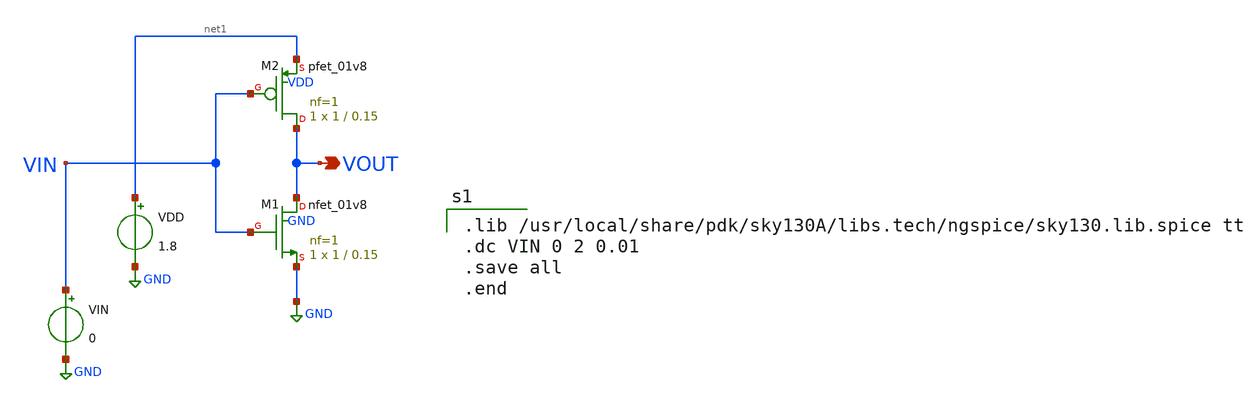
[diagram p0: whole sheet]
** sch_path: XSCHEM/inverter_simulation/inverter.sch
**.subckt inverter VOUT
*.opin VOUT
VDD net1 GND 1.8
VIN VIN GND 0
XM1 VOUT VIN GND GND sky130_fd_pr__nfet_01v8 L=0.15 W=1 nf=1 ad='int((nf+1)/2) * W/nf * 0.29' as='int((nf+2)/2) * W/nf * 0.29'
+ pd='2*int((nf+1)/2) * (W/nf + 0.29)' ps='2*int((nf+2)/2) * (W/nf + 0.29)' nrd='0.29 / W' nrs='0.29 / W'
+ sa=0 sb=0 sd=0 mult=1 m=1
XM2 VOUT VIN net1 VDD sky130_fd_pr__pfet_01v8 L=0.15 W=1 nf=1 ad='int((nf+1)/2) * W/nf * 0.29' as='int((nf+2)/2) * W/nf * 0.29'
+ pd='2*int((nf+1)/2) * (W/nf + 0.29)' ps='2*int((nf+2)/2) * (W/nf + 0.29)' nrd='0.29 / W' nrs='0.29 / W'
+ sa=0 sb=0 sd=0 mult=1 m=1
**** begin user architecture code

.lib /usr/local/share/pdk/sky130A/libs.tech/ngspice/sky130.lib.spice tt
.dc VIN 0 2 0.01
.save all
.end

**** end user architecture code
**.ends
.GLOBAL GND
.end
